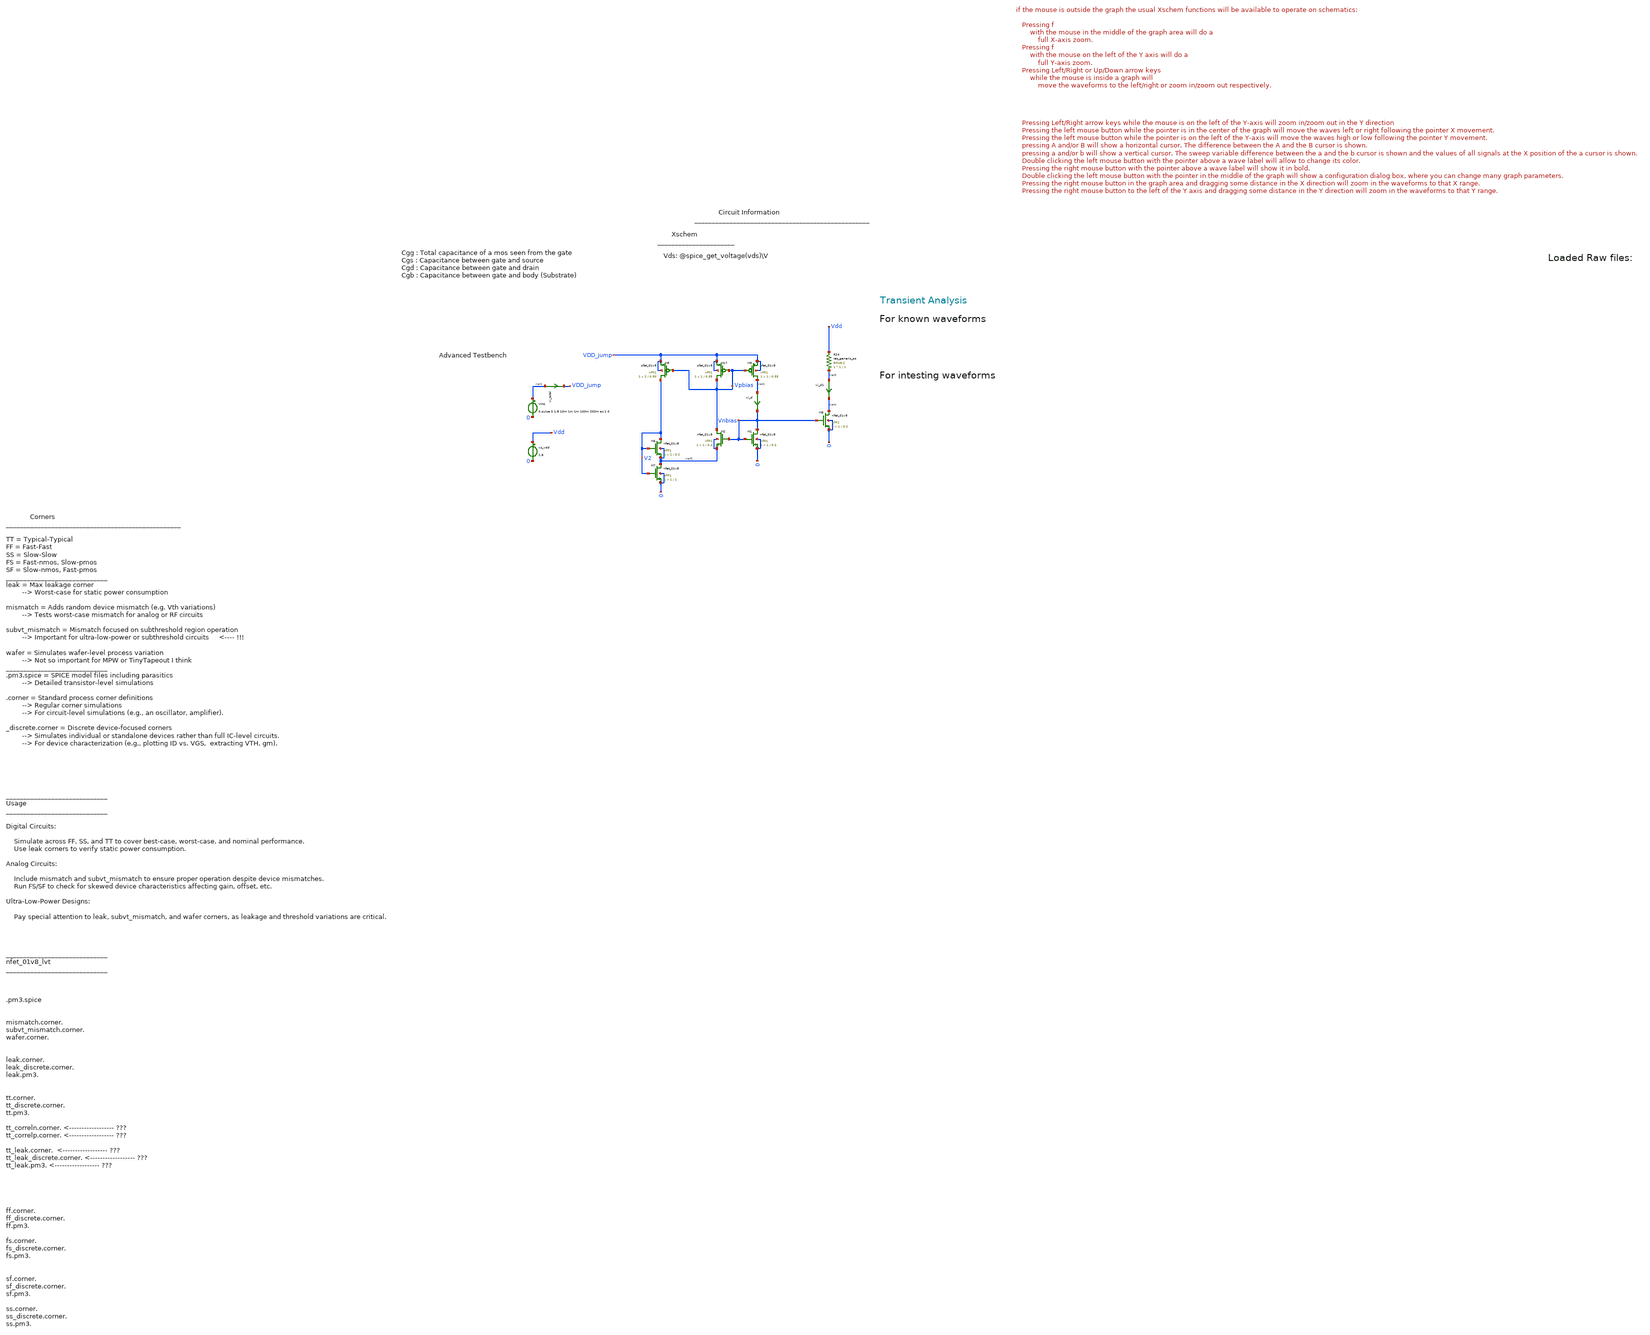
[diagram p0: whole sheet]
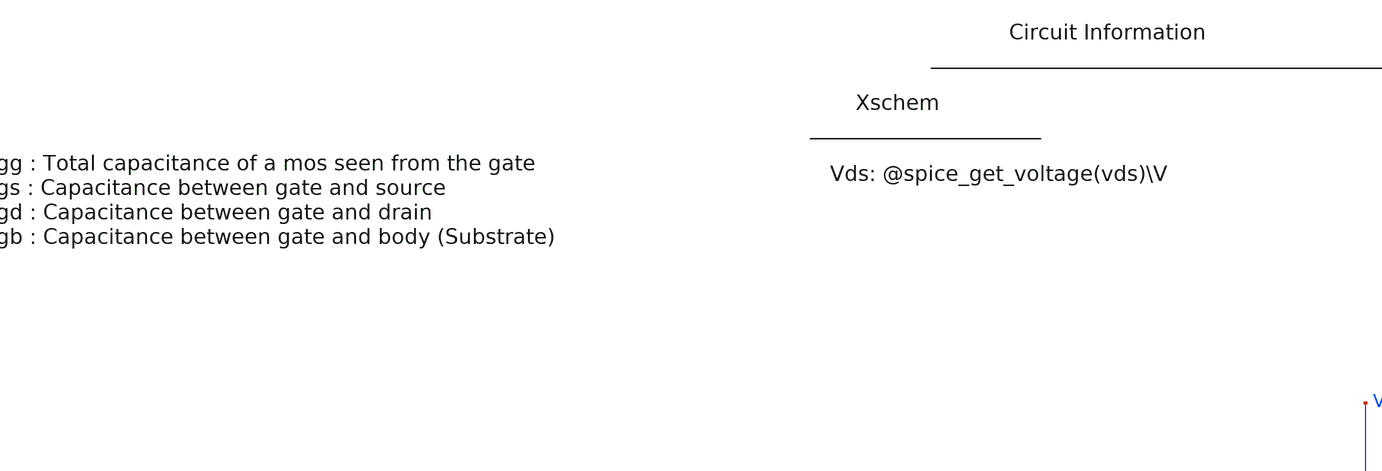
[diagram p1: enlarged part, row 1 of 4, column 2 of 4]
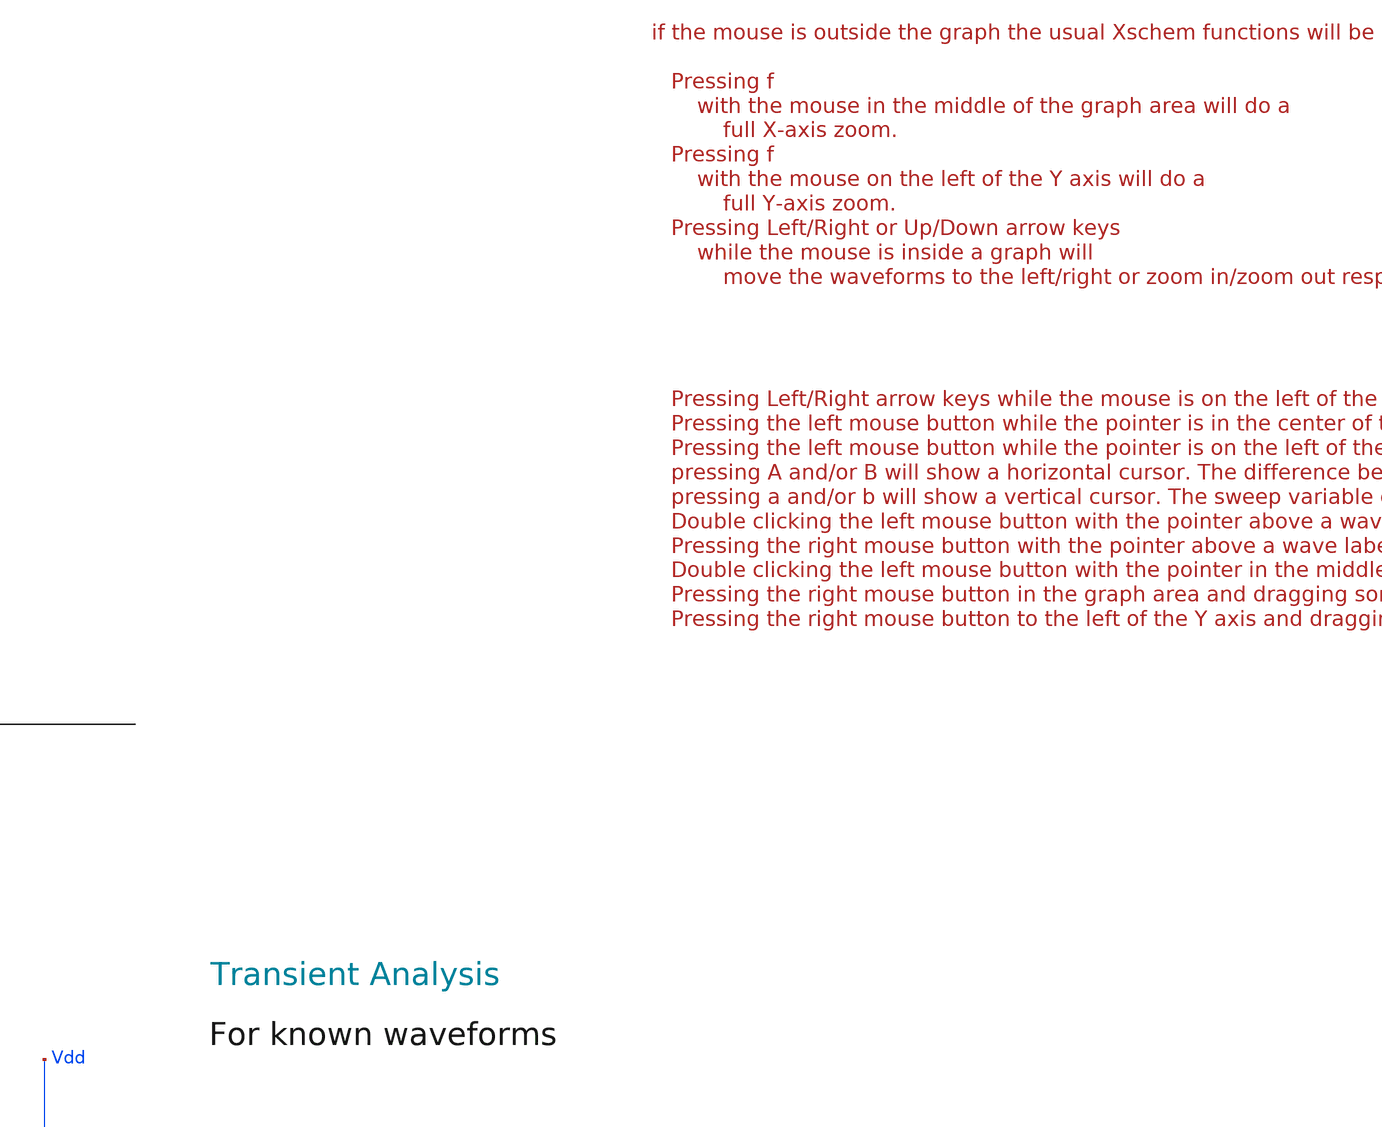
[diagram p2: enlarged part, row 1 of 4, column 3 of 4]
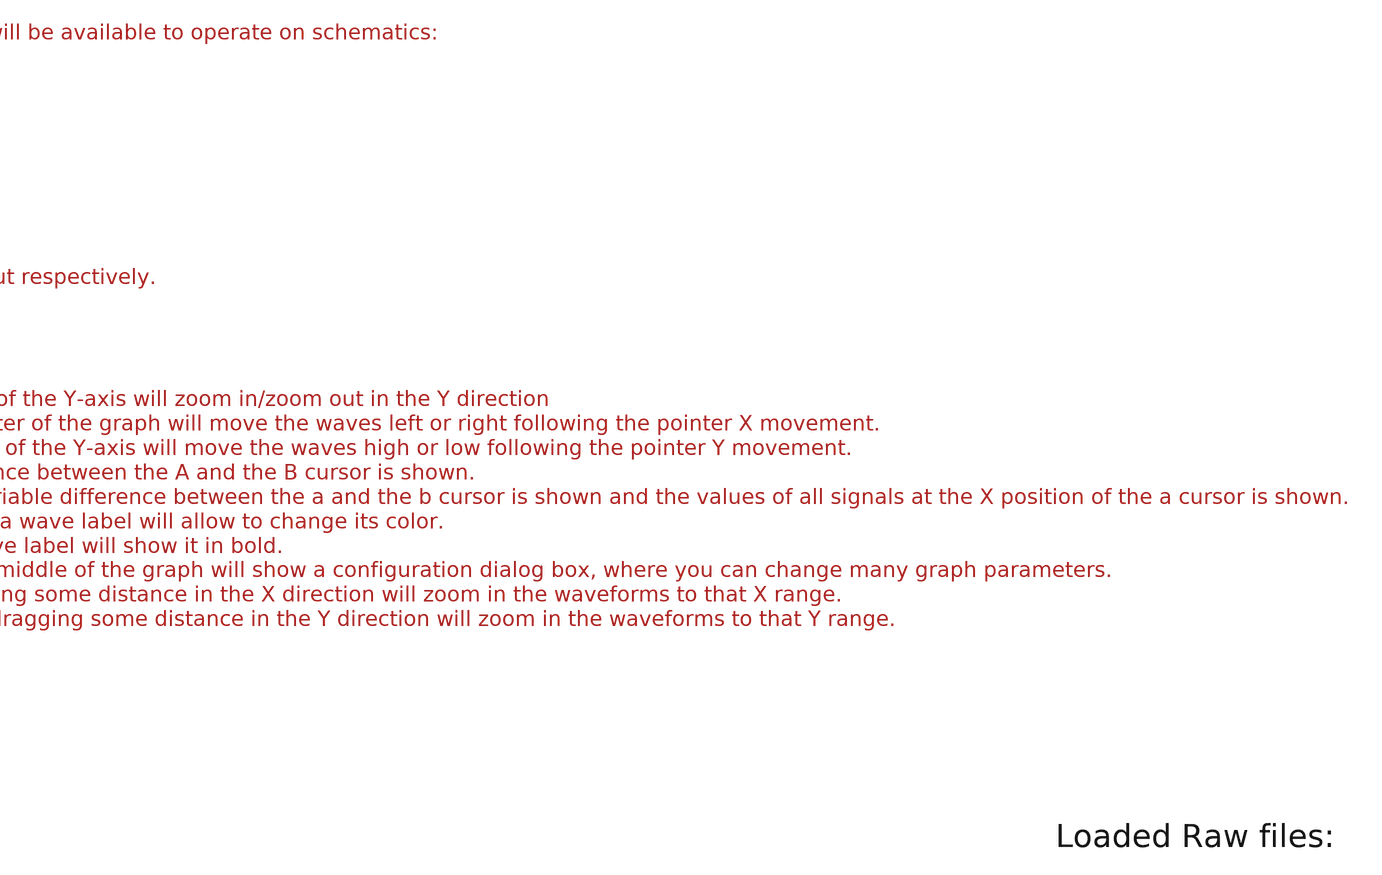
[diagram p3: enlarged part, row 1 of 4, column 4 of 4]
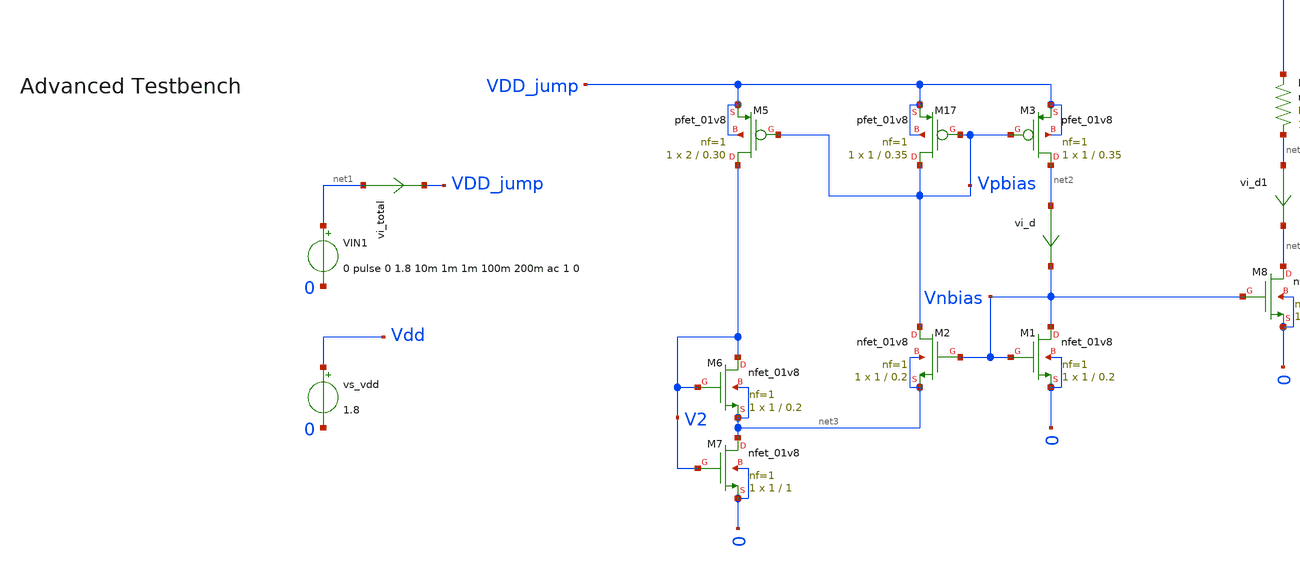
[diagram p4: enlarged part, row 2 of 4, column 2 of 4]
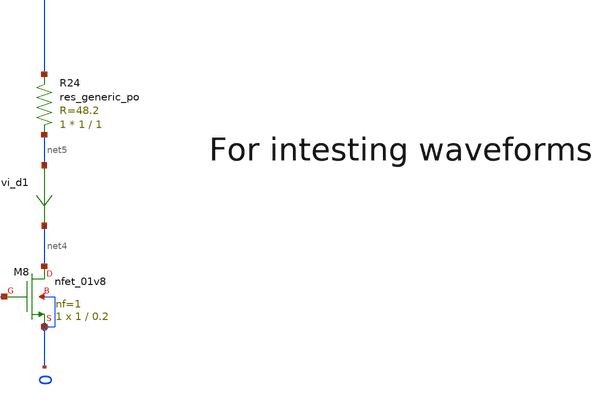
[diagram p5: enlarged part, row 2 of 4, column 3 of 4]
** sch_path: tt10-hdl/tt_um_test_commit/xschem/T2/biasGen/Z_old/weakInv_currSrc_Kushwaha_tb.sch
* Copyright (C) 1998-2024 Stefan Frederik Schippers
* This program is free software; you can redistribute it and/or modify
* it under the terms of the GNU General Public License as published by
* the Free Software Foundation; either version 2 of the License, or
* (at your option) any later version.
* This program is distributed in the hope that it will be useful,
* but WITHOUT ANY WARRANTY; without even the implied warranty of
* MERCHANTABILITY or FITNESS FOR A PARTICULAR PURPOSE.  See the
* GNU General Public License for more details.
* You should have received a copy of the GNU General Public License
* along with this program; if not, write to the Free Software
**.subckt weakInv_currSrc_Kushwaha_tb
VIN1 net1 0 0 pulse 0 1.8 10m 1m 1m 100m 200m ac 1 0
vi_total net1 VDD_jump 0
.save i(vi_total)
XM17 Vpbias Vpbias VDD_jump VDD_jump sky130_fd_pr__pfet_01v8 L=0.35 W=1 nf=1 ad='int((nf+1)/2) * W/nf * 0.29'
+ as='int((nf+2)/2) * W/nf * 0.29' pd='2*int((nf+1)/2) * (W/nf + 0.29)' ps='2*int((nf+2)/2) * (W/nf + 0.29)'
+ nrd='0.29 / W' nrs='0.29 / W' sa=0 sb=0 sd=0 mult=1 m=1
XM3 net2 Vpbias VDD_jump VDD_jump sky130_fd_pr__pfet_01v8 L=0.35 W=1 nf=1 ad='int((nf+1)/2) * W/nf * 0.29'
+ as='int((nf+2)/2) * W/nf * 0.29' pd='2*int((nf+1)/2) * (W/nf + 0.29)' ps='2*int((nf+2)/2) * (W/nf + 0.29)'
+ nrd='0.29 / W' nrs='0.29 / W' sa=0 sb=0 sd=0 mult=1 m=1
XM5 V2 Vpbias VDD_jump VDD_jump sky130_fd_pr__pfet_01v8 L=0.30 W=2 nf=1 ad='int((nf+1)/2) * W/nf * 0.29'
+ as='int((nf+2)/2) * W/nf * 0.29' pd='2*int((nf+1)/2) * (W/nf + 0.29)' ps='2*int((nf+2)/2) * (W/nf + 0.29)'
+ nrd='0.29 / W' nrs='0.29 / W' sa=0 sb=0 sd=0 mult=1 m=1
XM2 Vpbias Vnbias net3 net3 sky130_fd_pr__nfet_01v8 L=0.2 W=1 nf=1 ad='int((1 + 1)/2) * 1 / 1 * 0.29'
+ as='int((1 + 2)/2) * 1 / 1 * 0.29' pd='2*int((1 + 1)/2) * (1 / 1 + 0.29)' ps='2*int((1 + 2)/2) * (1 / 1 + 0.29)'
+ nrd='0.29 / 1 ' nrs='0.29 / 1 ' sa=0 sb=0 sd=0 mult=1 m=1
XM1 Vnbias Vnbias 0 0 sky130_fd_pr__nfet_01v8 L=0.2 W=1 nf=1 ad='int((1 + 1)/2) * 1 / 1 * 0.29' as='int((1 + 2)/2) * 1 / 1 * 0.29'
+ pd='2*int((1 + 1)/2) * (1 / 1 + 0.29)' ps='2*int((1 + 2)/2) * (1 / 1 + 0.29)' nrd='0.29 / 1 ' nrs='0.29 / 1 '
+ sa=0 sb=0 sd=0 mult=1 m=1
XM6 V2 V2 net3 net3 sky130_fd_pr__nfet_01v8 L=0.2 W=1 nf=1 ad='int((1 + 1)/2) * 1 / 1 * 0.29' as='int((1 + 2)/2) * 1 / 1 * 0.29'
+ pd='2*int((1 + 1)/2) * (1 / 1 + 0.29)' ps='2*int((1 + 2)/2) * (1 / 1 + 0.29)' nrd='0.29 / 1 ' nrs='0.29 / 1 '
+ sa=0 sb=0 sd=0 mult=1 m=1
XM7 net3 V2 0 0 sky130_fd_pr__nfet_01v8 L=1 W=1 nf=1 ad='int((1 + 1)/2) * 1 / 1 * 0.29' as='int((1 + 2)/2) * 1 / 1 * 0.29'
+ pd='2*int((1 + 1)/2) * (1 / 1 + 0.29)' ps='2*int((1 + 2)/2) * (1 / 1 + 0.29)' nrd='0.29 / 1 ' nrs='0.29 / 1 '
+ sa=0 sb=0 sd=0 mult=1 m=1
vi_d net2 Vnbias 0
.save i(vi_d)
vs_vdd Vdd 0 1.8
XM8 net4 Vnbias 0 0 sky130_fd_pr__nfet_01v8 L=0.2 W=1 nf=1 ad='int((1 + 1)/2) * 1 / 1 * 0.29' as='int((1 + 2)/2) * 1 / 1 * 0.29'
+ pd='2*int((1 + 1)/2) * (1 / 1 + 0.29)' ps='2*int((1 + 2)/2) * (1 / 1 + 0.29)' nrd='0.29 / 1 ' nrs='0.29 / 1 '
+ sa=0 sb=0 sd=0 mult=1 m=1
XR24 net5 Vdd sky130_fd_pr__res_generic_po W=1 L=1 m=1
vi_d1 net5 net4 0
.save i(vi_d1)
**** begin user architecture code



.temp 30

*.option gmin=5n
*.option scale=1e-6
.option wnflag=1
.option savecurrents

.save all
.control
  save all alli

  save @m.xm1.msky130_fd_pr__nfet_01v8[gm]
  save @m.xm1.msky130_fd_pr__nfet_01v8[id]
  save @m.xm1.msky130_fd_pr__nfet_01v8[vgs]

  save @m.xm1.msky130_fd_pr__nfet_01v8[cgg]
  save @m.xm1.msky130_fd_pr__nfet_01v8[cgs]
  save @m.xm1.msky130_fd_pr__nfet_01v8[cgdo]
  save @m.xm1.msky130_fd_pr__nfet_01v8[cgb]

  save @m.xm1.msky130_fd_pr__nfet_01v8[vds]
  save @m.xm1.msky130_fd_pr__nfet_01v8[vdsat]
  save @m.xm1.msky130_fd_pr__nfet_01v8[vth]


  save @m.xm1.msky130_fd_pr__nfet_01v8[leff]
  save @m.xm1.msky130_fd_pr__nfet_01v8[weff]
  save @m.xm1.msky130_fd_pr__nfet_01v8[gds]
  save @m.xm1.msky130_fd_pr__nfet_01v8[l]
  save @m.xm1.msky130_fd_pr__nfet_01v8[w]
  save @m.xm1.msky130_fd_pr__nfet_01v8[gm]
  save @m.xm1.msky130_fd_pr__nfet_01v8[gm]
  save @m.xm1.msky130_fd_pr__nfet_01v8[gm]
  save @m.xm1.msky130_fd_pr__nfet_01v8[gm]
  save @m.xm1.msky130_fd_pr__nfet_01v8[gm]



  *dc v_dev_vds 0 1.8 0.005 v_dev_vgs 0 1.8 0.2
  *write nmos_tb.raw




  tran 1m 50m
  write nmos_tb_tran.raw

  op
  set appendwrite
  write nmos_tb_tran.raw






  *quit 0




.endc





** opencircuitdesign pdks install
.lib $::SKYWATER_MODELS/sky130.lib.spice tt
.include $::SKYWATER_STDCELLS/sky130_fd_sc_hd.spice


**** end user architecture code
**.ends
.end
